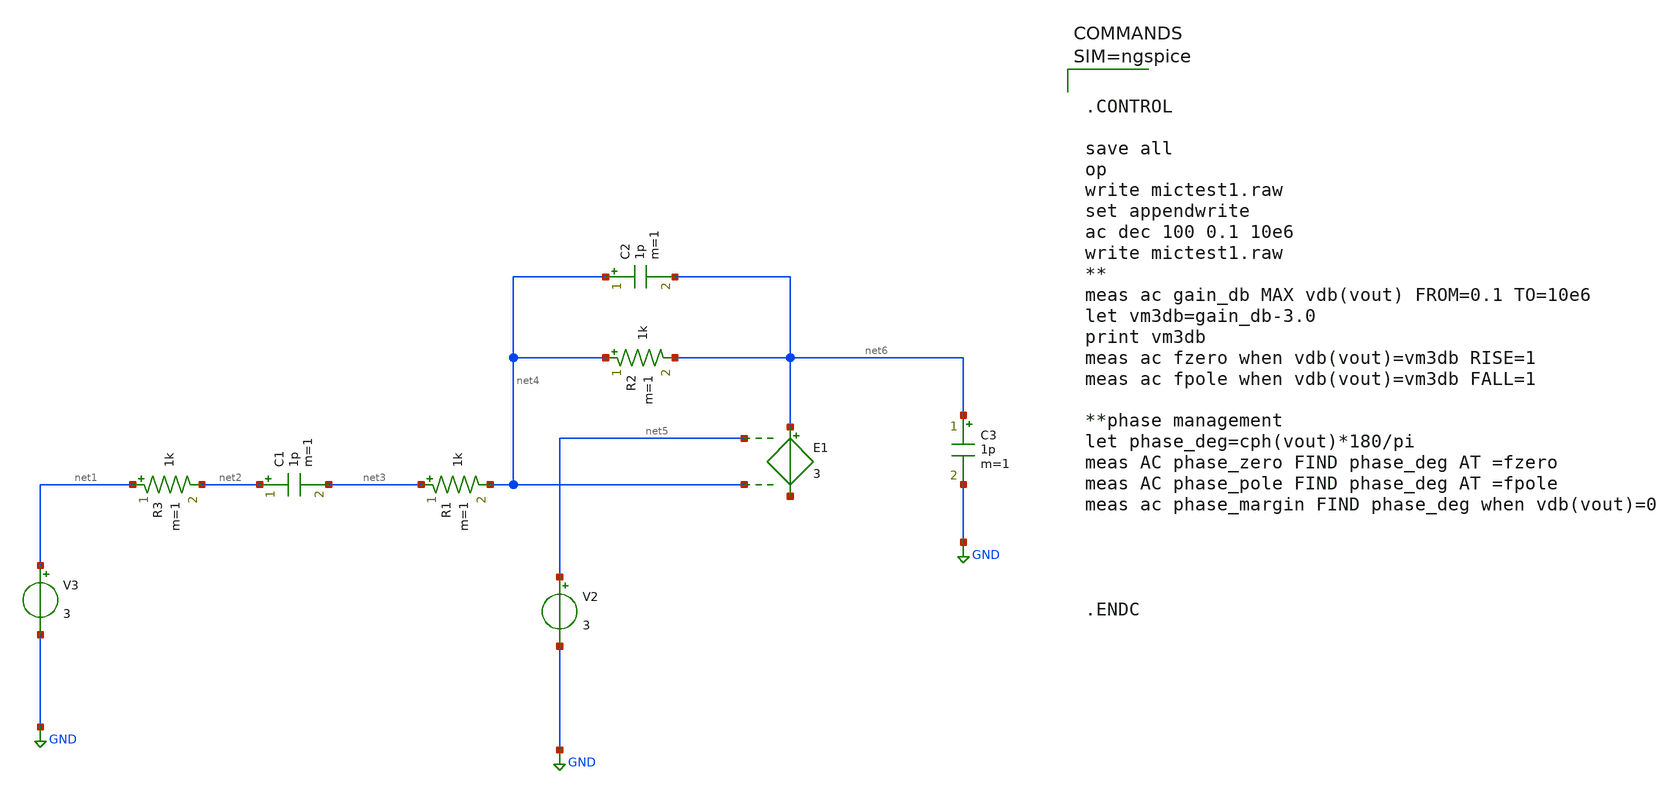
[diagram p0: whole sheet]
** sch_path: work/xschem/mictest2.sch
**.subckt mictest2
E1 net6 net7 net5 net4 3
R1 net3 net4 1k m=1
C1 net2 net3 1p m=1
V2 net5 GND 3
R2 net4 net6 1k m=1
C2 net4 net6 1p m=1
C3 net6 GND 1p m=1
R3 net1 net2 1k m=1
V3 net1 GND 3
**** begin user architecture code



.CONTROL

save all
op
write mictest1.raw
set appendwrite
ac dec 100 0.1 10e6
write mictest1.raw
**
meas ac gain_db MAX vdb(vout) FROM=0.1 TO=10e6
let vm3db=gain_db-3.0
print vm3db
meas ac fzero when vdb(vout)=vm3db RISE=1
meas ac fpole when vdb(vout)=vm3db FALL=1

**phase management
let phase_deg=cph(vout)*180/pi
meas AC phase_zero FIND phase_deg AT =fzero
meas AC phase_pole FIND phase_deg AT =fpole
meas ac phase_margin FIND phase_deg when vdb(vout)=0




.ENDC



**** end user architecture code
**.ends
.GLOBAL GND
.end
